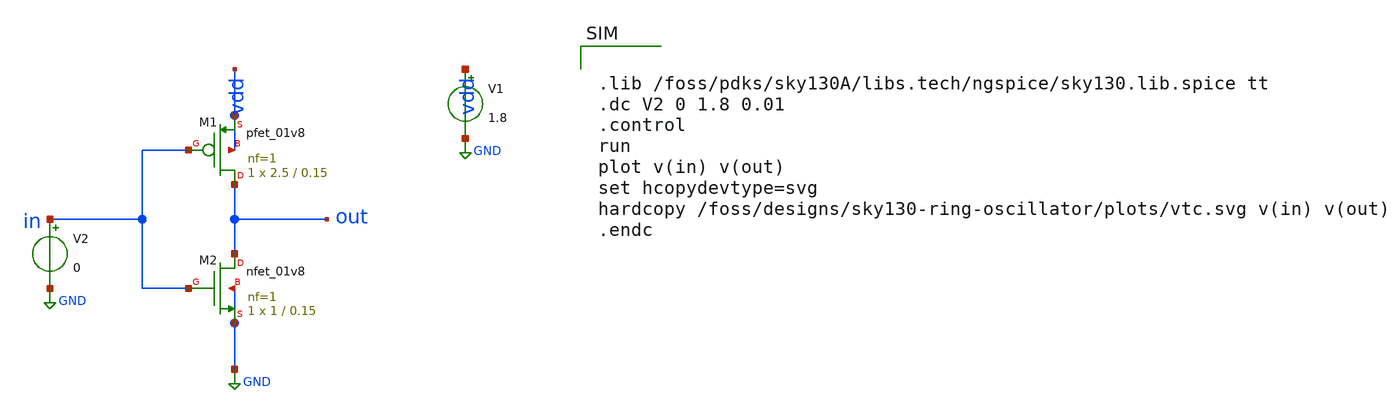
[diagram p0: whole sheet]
** sch_path: xschem/inverter.sch
**.subckt inverter
XM1 out in vdd vdd sky130_fd_pr__pfet_01v8 L=0.15 W=2.5 nf=1 ad='int((1 + 1)/2) * 2.5 / 1 * 0.29' as='int((1 + 2)/2) * 2.5 / 1 * 0.29'
+ pd='2*int((1 + 1)/2) * (2.5 / 1 + 0.29)' ps='2*int((1 + 2)/2) * (2.5 / 1 + 0.29)' nrd='0.29 / 2.5 ' nrs='0.29 / 2.5 '
+ sa=0 sb=0 sd=0 mult=1 m=1
XM2 out in GND GND sky130_fd_pr__nfet_01v8 L=0.15 W=1 nf=1 ad='int((1 + 1)/2) * 1 / 1 * 0.29' as='int((1 + 2)/2) * 1 / 1 * 0.29'
+ pd='2*int((1 + 1)/2) * (1 / 1 + 0.29)' ps='2*int((1 + 2)/2) * (1 / 1 + 0.29)' nrd='0.29 / 1 ' nrs='0.29 / 1 '
+ sa=0 sb=0 sd=0 mult=1 m=1
V1 vdd GND 1.8
V2 in GND 0
**** begin user architecture code


.lib /foss/pdks/sky130A/libs.tech/ngspice/sky130.lib.spice tt
.dc V2 0 1.8 0.01
.control
run
plot v(in) v(out)
set hcopydevtype=svg
hardcopy /foss/designs/sky130-ring-oscillator/plots/vtc.svg v(in) v(out)
.endc


**** end user architecture code
**.ends
.GLOBAL GND
.end
